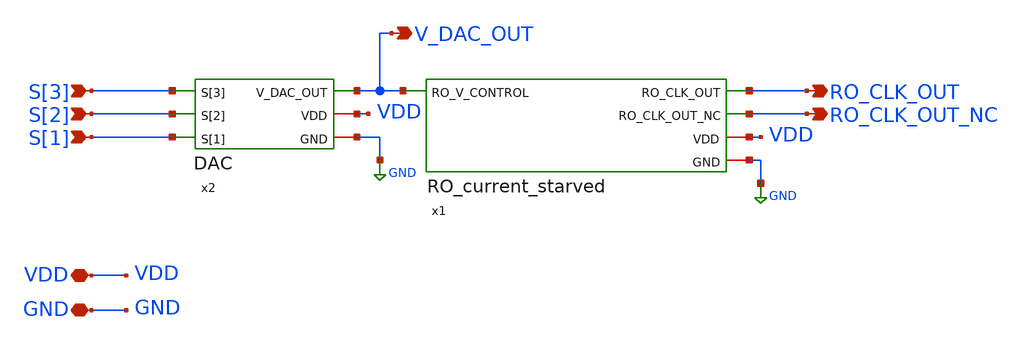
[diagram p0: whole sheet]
** sch_path: src/analog_source_files/RO_DAC.sch
**.subckt RO_DAC RO_CLK_OUT RO_CLK_OUT_NC S[3] S[2] S[1] VDD GND V_DAC_OUT
*.opin RO_CLK_OUT
*.opin RO_CLK_OUT_NC
*.ipin S[3]
*.ipin S[2]
*.ipin S[1]
*.iopin VDD
*.iopin GND
*.opin V_DAC_OUT
x1 RO_CLK_OUT V_DAC_OUT VDD GND RO_CLK_OUT_NC RO_current_starved
x2 S[3] S[1] S[2] V_DAC_OUT VDD GND DAC
**.ends
.GLOBAL GND
.end
